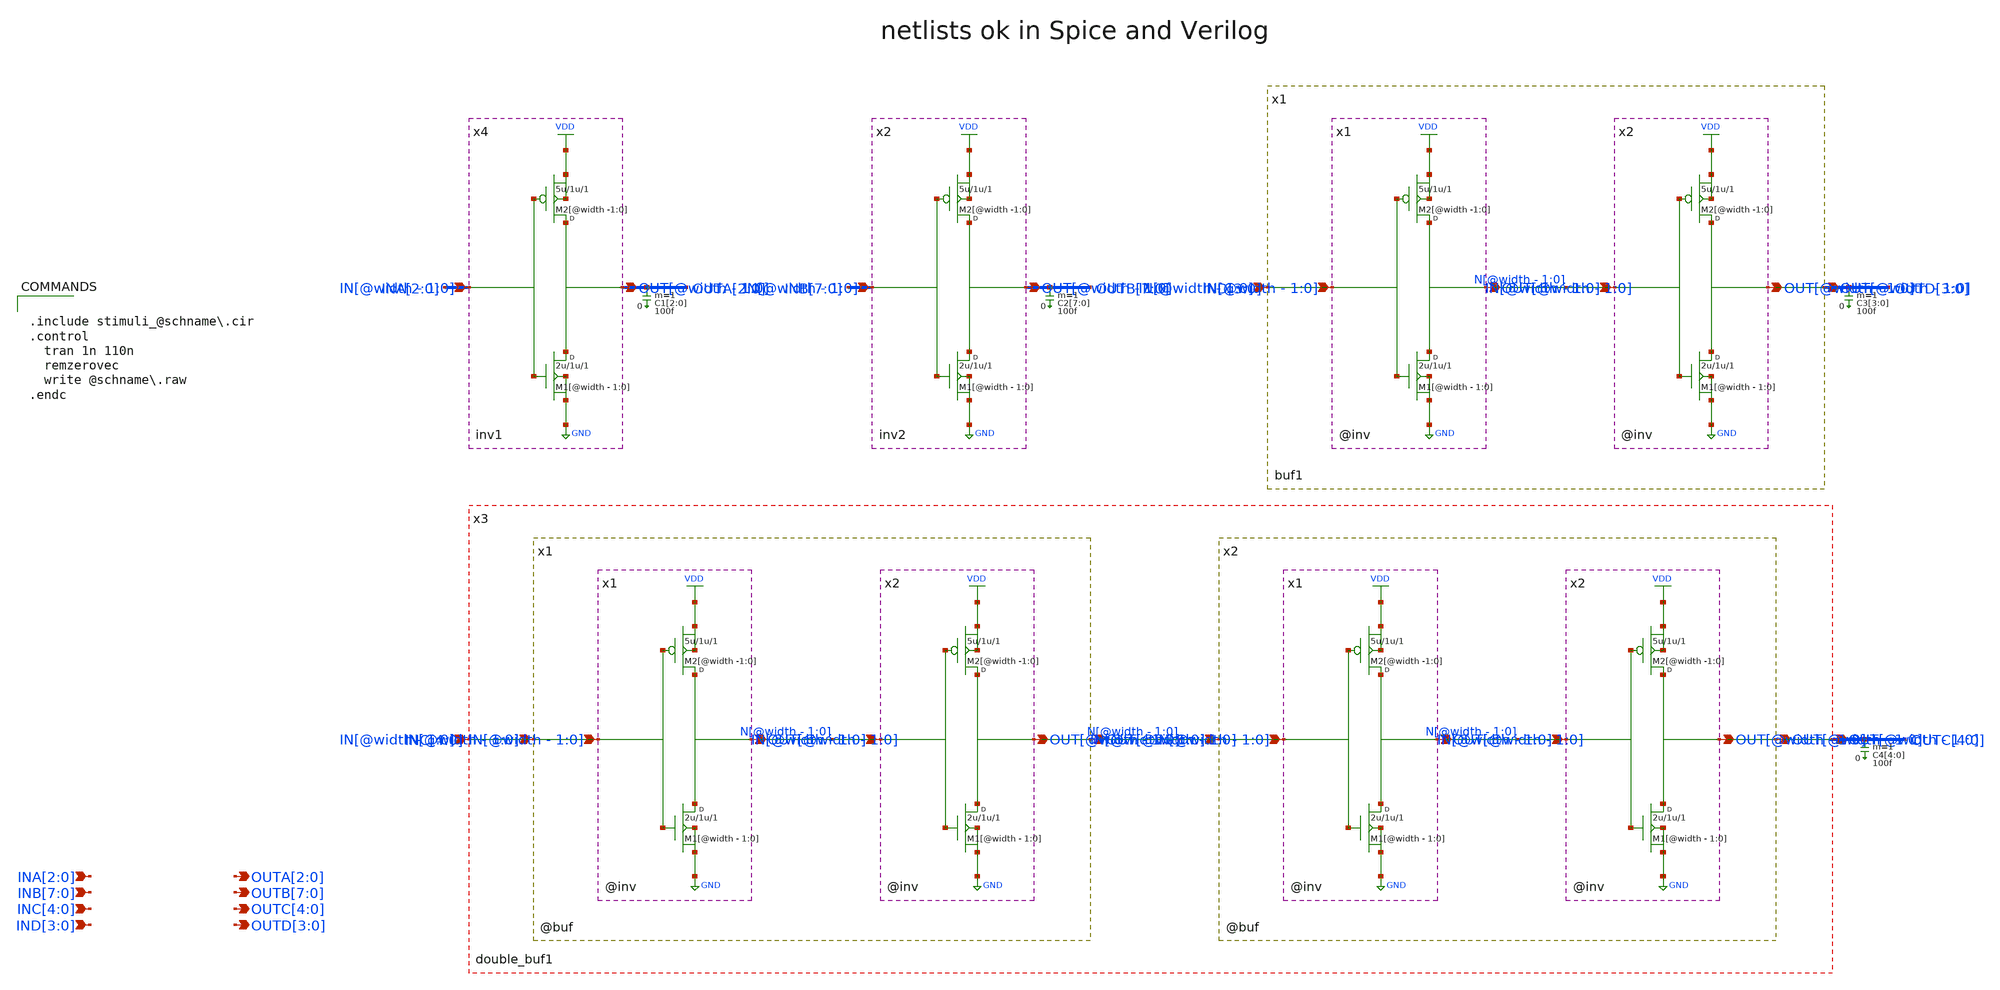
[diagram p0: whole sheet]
** sch_path: xschem_library/examples/test_parametric_ports/tb_param_ports_lcc.sch
**.subckt tb_param_ports_lcc IND[3],IND[2],IND[1],IND[0] INC[4],INC[3],INC[2],INC[1],INC[0]
*+ INB[7],INB[6],INB[5],INB[4],INB[3],INB[2],INB[1],INB[0] INA[2],INA[1],INA[0] OUTD[3],OUTD[2],OUTD[1],OUTD[0] OUTC[4],OUTC[3],OUTC[2],OUTC[1],OUTC[0]
*+ OUTB[7],OUTB[6],OUTB[5],OUTB[4],OUTB[3],OUTB[2],OUTB[1],OUTB[0] OUTA[2],OUTA[1],OUTA[0]
*.ipin IND[3],IND[2],IND[1],IND[0]
*.ipin INC[4],INC[3],INC[2],INC[1],INC[0]
*.ipin INB[7],INB[6],INB[5],INB[4],INB[3],INB[2],INB[1],INB[0]
*.ipin INA[2],INA[1],INA[0]
*.opin OUTD[3],OUTD[2],OUTD[1],OUTD[0]
*.opin OUTC[4],OUTC[3],OUTC[2],OUTC[1],OUTC[0]
*.opin OUTB[7],OUTB[6],OUTB[5],OUTB[4],OUTB[3],OUTB[2],OUTB[1],OUTB[0]
*.opin OUTA[2],OUTA[1],OUTA[0]
x2 OUTB[7] OUTB[6] OUTB[5] OUTB[4] OUTB[3] OUTB[2] OUTB[1] OUTB[0] INB[7] INB[6] INB[5] INB[4]
+ INB[3] INB[2] INB[1] INB[0] inv2
x4 OUTA[2] OUTA[1] OUTA[0] INA[2] INA[1] INA[0] inv1
x1 OUTD[3] OUTD[2] OUTD[1] OUTD[0] IND[3] IND[2] IND[1] IND[0] buf1
x3 OUTC[4] OUTC[3] OUTC[2] OUTC[1] OUTC[0] INC[4] INC[3] INC[2] INC[1] INC[0] double_buf1
C1[2] OUTA[2] 0 100f m=1
C1[1] OUTA[1] 0 100f m=1
C1[0] OUTA[0] 0 100f m=1
C2[7] OUTB[7] 0 100f m=1
C2[6] OUTB[6] 0 100f m=1
C2[5] OUTB[5] 0 100f m=1
C2[4] OUTB[4] 0 100f m=1
C2[3] OUTB[3] 0 100f m=1
C2[2] OUTB[2] 0 100f m=1
C2[1] OUTB[1] 0 100f m=1
C2[0] OUTB[0] 0 100f m=1
C3[3] OUTD[3] 0 100f m=1
C3[2] OUTD[2] 0 100f m=1
C3[1] OUTD[1] 0 100f m=1
C3[0] OUTD[0] 0 100f m=1
C4[4] OUTC[4] 0 100f m=1
C4[3] OUTC[3] 0 100f m=1
C4[2] OUTC[2] 0 100f m=1
C4[1] OUTC[1] 0 100f m=1
C4[0] OUTC[0] 0 100f m=1
**** begin user architecture code


.include stimuli_@schname\.cir
.control
  tran 1n 110n
  remzerovec
  write @schname\.raw
.endc




** From the ngspice distribution:
** https://sourceforge.net/p/ngspice/ngspice/ci/master/tree/examples/mos/modelcard.nmos
** https://sourceforge.net/p/ngspice/ngspice/ci/master/tree/examples/mos/modelcard.pmos

.model cmosn NMOS Level=        49 version=3.3.0 Tnom=27.0 Nch= 2.498E+17  Tox=9E-09 Xj=1.00000E-07
+ Lint=9.36e-8 Wint=1.47e-7 Vth0= .6322    K1= .756  K2= -3.83e-2  K3= -2.612 Dvt0= 2.812  Dvt1= 0.462
+  Dvt2=-9.17e-2 Nlx= 3.52291E-08  W0= 1.163e-6 K3b= 2.233 Vsat= 86301.58  Ua= 6.47e-9  Ub= 4.23e-18
+  Uc=-4.706281E-11 Rdsw= 650  U0= 388.3203 wr=1 A0= .3496967 Ags=.1    B0=0.546    B1= 1 Dwg = -6.0E-09 Dwb =
+ -3.56E-09 Prwb = -.213 Keta=-3.605872E-02  A1= 2.778747E-02  A2= .9 Voff=-6.735529E-02  NFactor= 1.139926
+  Cit= 1.622527E-04 Cdsc=-2.147181E-05 Cdscb= 0  Dvt0w =  0 Dvt1w =  0 Dvt2w =  0 Cdscd =  0 Prwg =  0
+ Eta0= 1.0281729E-02  Etab=-5.042203E-03 Dsub= .31871233 Pclm= 1.114846  Pdiblc1= 2.45357E-03  Pdiblc2=
+ 6.406289E-03 Drout= .31871233  Pscbe1= 5000000  Pscbe2= 5E-09 Pdiblcb = -.234 Pvag= 0 delta=0.01 Wl =  0 Ww =
+ -1.420242E-09 Wwl =  0 Wln =  0 Wwn =  .2613948 Ll =  1.300902E-10 Lw =  0 Lwl =  0 Lln =  .316394 Lwn =  0
+ kt1=-.3  kt2=-.051 At= 22400 Ute=-1.48 Ua1= 3.31E-10  Ub1= 2.61E-19 Uc1= -3.42e-10 Kt1l=0 Prt=764.3
+ vgs_max=4 vds_max=4 vbs_max=4

.model cmosp PMOS Level=        49 version=3.3.0 Tnom=27.0 Nch= 3.533024E+17  Tox=9E-09
+ Xj=1.00000E-07 Lint=6.23e-8 Wint=1.22e-7 Vth0=-.6732829 K1= .8362093  K2=-8.606622E-02  K3= 1.82 Dvt0= 1.903801
+  Dvt1= .5333922  Dvt2=-.1862677 Nlx= 1.28e-8  W0= 2.1e-6 K3b= -0.24 Prwg=-0.001 Prwb=-0.323 Vsat= 103503.2
+  Ua= 1.39995E-09  Ub= 1.e-19  Uc=-2.73e-11 Rdsw= 460  U0= 138.7609 A0= .4716551 Ags=0.12
+ Keta=-1.871516E-03  A1= .3417965  A2= 0.83 Voff=-.074182  NFactor= 1.54389  Cit=-1.015667E-03 Cdsc= 8.937517E-04
+ Cdscb= 1.45e-4  Cdscd=1.04e-4 Dvt0w=0.232 Dvt1w=4.5e6 Dvt2w=-0.0023 Eta0= 6.024776E-02  Etab=-4.64593E-03
+ Dsub= .23222404 Pclm= .989  Pdiblc1= 2.07418E-02  Pdiblc2= 1.33813E-3 Drout= .3222404  Pscbe1= 118000
+  Pscbe2= 1E-09 Pvag= 0 kt1= -0.25  kt2= -0.032 prt=64.5 At= 33000 Ute= -1.5 Ua1= 4.312e-9 Ub1= 6.65e-19
+  Uc1= 0 Kt1l=0 vgs_max=4 vds_max=4 vbs_max=4


**** end user architecture code
**.ends
.end
